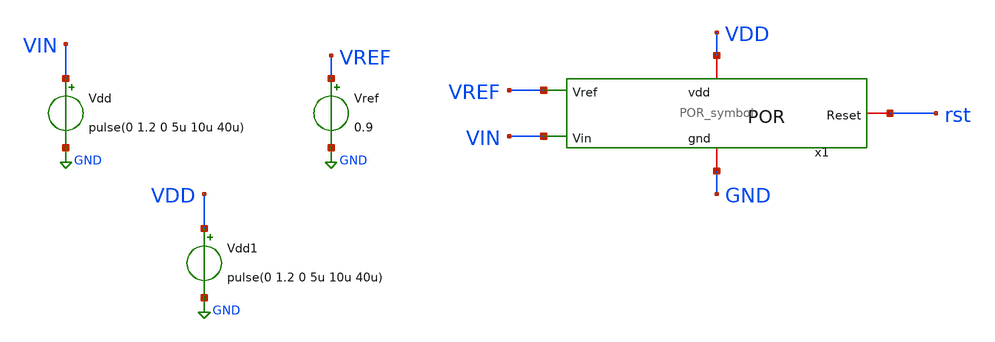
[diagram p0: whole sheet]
** sch_path: dependencies/POR/POR-main/testbenches/corners/xschem/POR_Corners.sch
**.subckt POR_Corners
Vref VREF GND 0.9
Vdd VIN GND pulse(0 1.2 0 5u 10u 40u)
Vdd1 VDD GND pulse(0 1.2 0 5u 10u 40u)
x1 VDD VREF VIN rst GND POR_symbol
**** begin user architecture code


.control
.save all

tran 2n 80u
plot rst vdd


.endc




** IHP models
.lib cornerMOSlv.lib mos_tt

.lib cornerHBT.lib hbt_typ
.lib cornerRES.lib res_typ
.lib cornerCAP.lib cap_typ
.include sg13g2_stdcell.spice


**** end user architecture code
**.ends

* expanding   symbol:  /foss/designs/projet/HABIS/ip/Por/xschem/POR_symbol.sym # of pins=5
** sym_path: dependencies/POR/POR-main/testbenches/tran_mc/xschem/POR_symbol.sym
** sch_path: dependencies/POR/POR-main/testbenches/tran_mc/xschem/POR_symbol.sch
.subckt POR_symbol vdd Vref Vin Reset gnd
*.iopin vdd
*.iopin gnd
*.ipin Vin
*.ipin Vref
*.iopin Reset
XM15 net7 net8 vdd vdd sg13_lv_pmos w=5.2u l=0.13u ng=1 m=1 mm_ok=1
XM16 net7 net3 gnd gnd sg13_lv_nmos w=0.52u l=0.13u ng=1 m=1 mm_ok=1
XM17 net8 net1 vdd vdd sg13_lv_pmos w=5.2u l=0.13u ng=2 m=1 mm_ok=1
XM18 net8 Vref net2 GND sg13_lv_nmos w=3.64u l=3.7u ng=1 m=1 mm_ok=1
XM19 net1 net1 vdd vdd sg13_lv_pmos w=5.2u l=0.13u ng=2 m=1 mm_ok=1
XM20 net1 Vin net2 GND sg13_lv_nmos w=3.64u l=3.7u ng=1 m=1 mm_ok=1
XM21 net2 net3 gnd gnd sg13_lv_nmos w=5.3u l=1.95u ng=1 m=1 mm_ok=1
XM22 net3 net3 gnd gnd sg13_lv_nmos w=0.15u l=0.15u ng=1 m=1 mm_ok=1
XM23 net6 net4 vdd vdd sg13_lv_pmos w=2.6u l=0.13u ng=1 m=1 mm_ok=1
XM24 Reset net4 net6 net6 sg13_lv_pmos w=2.6u l=0.13u ng=1 m=1 mm_ok=1
XM25 Reset net4 net5 Reset sg13_lv_nmos w=1.3u l=0.13u ng=1 m=1 mm_ok=1
XM26 net5 net4 gnd gnd sg13_lv_nmos w=1.3u l=0.13u ng=1 m=1 mm_ok=1
XM27 net6 Reset gnd vdd sg13_lv_pmos w=2.950u l=0.13u ng=1 m=1 mm_ok=1
XM28 net5 Reset vdd gnd sg13_lv_nmos w=2.950u l=0.13u ng=1 m=1 mm_ok=1
XR44 vdd net3 sub! rppd w=0.5e-6 l=330.60e-6 m=1 b=0 mm_ok=1
XC2 Reset gnd cap_cmim w=26.98e-6 l=26.98e-6 m=1 mm_ok=1
XC1 net4 gnd cap_cmim w=41.519e-6 l=41.519e-6 m=1 mm_ok=1
XR45 net4 net7 sub! rppd w=2e-6 l=7.45e-6 m=1 b=0 mm_ok=1
.ends

.GLOBAL GND
.end
